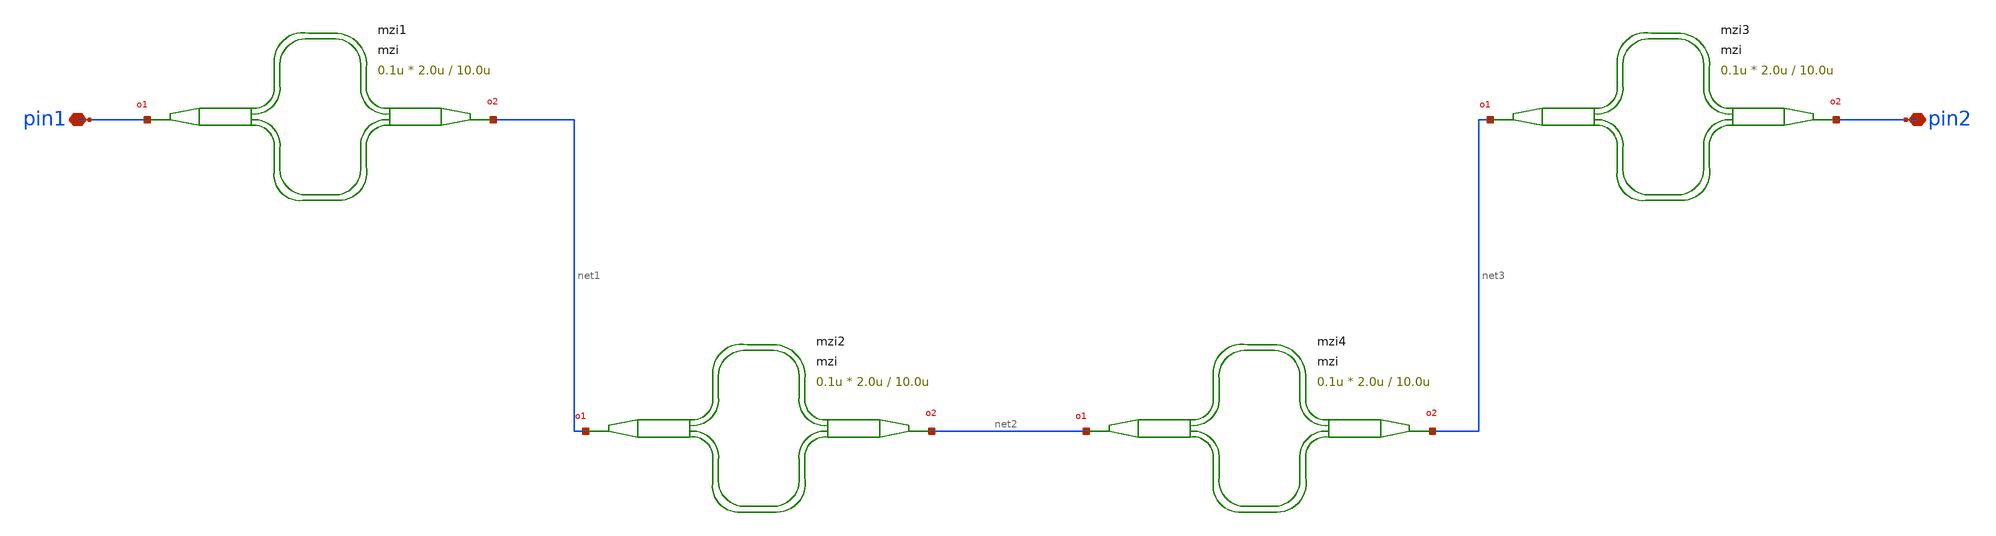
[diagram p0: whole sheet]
** sch_path: xschem/tests/test_sch/test_mzi.sch
* Copyright (c) 2024, Mabrains LLC
* Licensed under the GNU Lesser General Public License, Version 3.0 (the "License");
* you may not use this file except in compliance with the License.
* GNU Lesser General Public License
* Version 3, 29 June 2007
* This program is free software: you can redistribute it and/or modify
* it under the terms of the GNU Lesser General Public License as published
* by the Free Software Foundation, either version 3 of the License, or
* (at your option) any later version.
* This program is distributed in the hope that it will be useful,
* but WITHOUT ANY WARRANTY; without even the implied warranty of
* MERCHANTABILITY or FITNESS FOR A PARTICULAR PURPOSE.  See the
* GNU Lesser General Public License for more details.
* You should have received a copy of the GNU Lesser General Public License
* along with this program.  If not, see <https://www.gnu.org/licenses/>.
* SPDX-License-Identifier: LGPL-3.0
**.subckt test_mzi pin1 pin2
*.iopin pin1
*.iopin pin2
Pmzi2 net1 net2 mzi delta_length=10.0u length_y=2.0u length_x=0.1u
Pmzi1 pin1 net1 mzi delta_length=10.0u length_y=2.0u length_x=0.1u
Pmzi3 net3 pin2 mzi delta_length=10.0u length_y=2.0u length_x=0.1u
Pmzi4 net2 net3 mzi delta_length=10.0u length_y=2.0u length_x=0.1u
**.ends
.end
